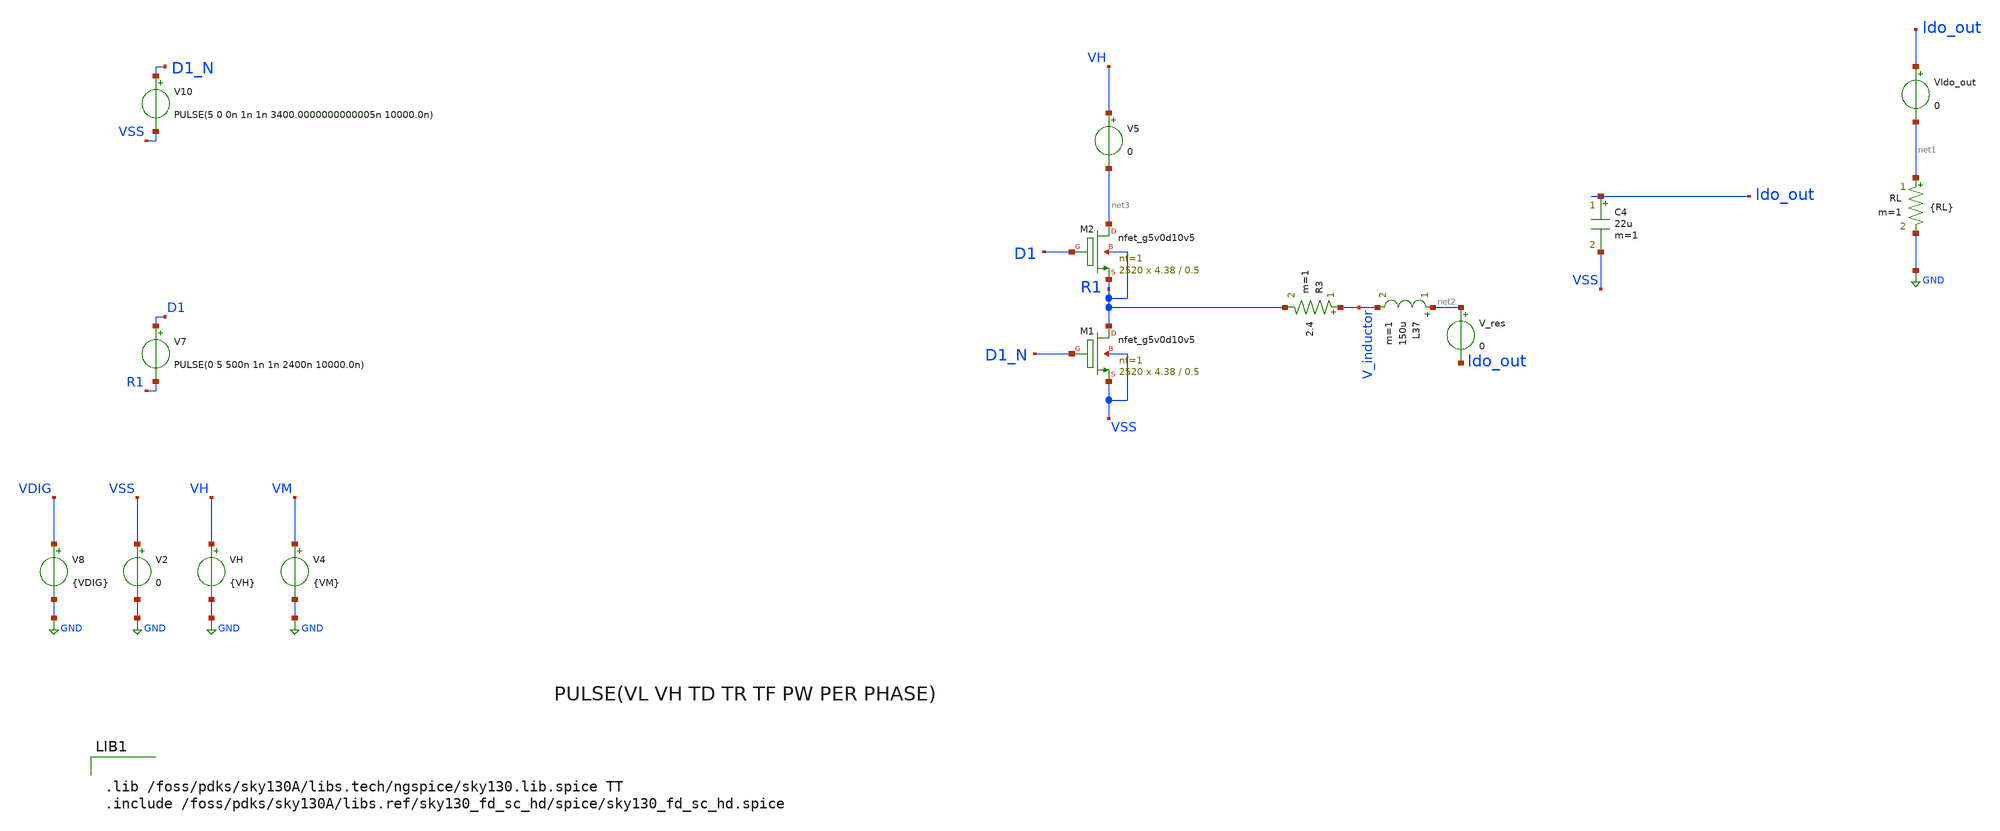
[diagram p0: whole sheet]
** sch_path: LS_boot_20230921/sch/tb_DCDC_wfilter_1core100KHznoCext_buckBOOT_eff_nols.sch
**.subckt tb_DCDC_wfilter_1core100KHznoCext_buckBOOT_eff_nols
V2 VSS GND 0
VH VH GND {VH}
V8 VDIG GND {VDIG}
V4 VM GND {VM}
C4 ldo_out VSS 22u m=1
RL net1 GND {RL} m=1
Vldo_out ldo_out net1 0
V7 D1 R1 PULSE(0 5 500n 1n 1n 2400n 10000.0n)
V10 D1_N VSS PULSE(5 0 0n 1n 1n 3400.0000000000005n 10000.0n)
L37 net2 V_inductor 150u m=1
R3 V_inductor R1 2.4 m=1
XM1 R1 D1_N VSS VSS sky130_fd_pr__nfet_g5v0d10v5 L=0.5 W=4.38 nf=1 ad='int((nf+1)/2) * W/nf * 0.29' as='int((nf+2)/2) * W/nf * 0.29'
+ pd='2*int((nf+1)/2) * (W/nf + 0.29)' ps='2*int((nf+2)/2) * (W/nf + 0.29)' nrd='0.29 / W' nrs='0.29 / W'
+ sa=0 sb=0 sd=0 mult=2520 m=2520
V5 VH net3 0
V_res net2 ldo_out 0
XM2 net3 D1 R1 R1 sky130_fd_pr__nfet_g5v0d10v5 L=0.5 W=4.38 nf=1 ad='int((nf+1)/2) * W/nf * 0.29' as='int((nf+2)/2) * W/nf * 0.29'
+ pd='2*int((nf+1)/2) * (W/nf + 0.29)' ps='2*int((nf+2)/2) * (W/nf + 0.29)' nrd='0.29 / W' nrs='0.29 / W'
+ sa=0 sb=0 sd=0 mult=2520 m=2520
**** begin user architecture code


.param VIN = 5
.param VDIG = 1.8
.param VH = 10
.param VM = 5
.param VBAT = 5
.param RL = 44
VGND VGND GND 0
VNB VNB GND 0
VPB VPB GND 1.8
VPWR VPWR GND 1.8

.option scale=1e-6
*.options itl4=25
*.options method=gear
*.option temp=80
.ic v(vout_core)=3
.ic v(V_inductor)=3
.ic v(V_res)=3
*.probe vd(MP2:G:S)
*.save all
*.save v(d1) v(d2) v(d1top_5v) v(d2_5v) v(d2bot_5v) v(d1bot_5v) v(vout) v(vout_core) v(vdd) v(vh) i(v1) i(v5) i(vmeas) v(v_cftop,v_cfbot)
.save v(D1) v(D2) v(D1_N) v(D2_N) v(VOUT_CORE) v(ldo_out) v(vh) i(v3) i(v10) i(v11) v(v_cftop,v_cfbot) v(D1,v_cftop) v(D2,vout_core) v(D2_N,v_cfbot) v(D1_Nv,VSS) v(v_out_ls1) v(v_out_ls2) v(d2_n,v_cfbot) v(D1_s) v(D2_s) v(D2_N_s) v(D1_N_s) v(V_res) i(v9) v(ldo_out)
.save v(neg) v(pos) i(vh) i(v_res) v(R1) v(Vboot) v(vfe) v(vre) v(vbat) i(vbat) v(v_inductor)
.save @m.xm4.msky130_fd_pr__nfet_g5v0d10v5[vds]
.param mc_mm_switch=0
.options savecurrents
.control
*set gmin = 1e-20
*save all
*tran 10n 3m
tran 10n 3m
*write DCDC_v1p4_5MHz_NMOS_PMOS.raw
*wrdata
*+ ~/Documents/Postdoc/chipathon2022/3LFCC_AC3E/xschem/dev_switches/DCDC_5V_FINAL/3LFCC_v1p4.txt tran.v(vout) tran.i(vmeas) tran.v(vdd) tran.i(v3) tran.v(vh) tran.i(v5)
*wrdata /foss/designs/personal/3LFCC_AC3E/xschem/hierarchy_sch/DCDC_5V_FINAL/3LFCC_v1p4.txt
*+ tran.v(vout_core) tran.i(v1)
*wrdata
*+ /foss/designs/personal/3LFCC_AC3E/xschem/testbench/TopModule/3LFCC_v1p5_topmodule_wfilter_jmtest.txt tran.v(vout_core) tran.i(v3) tran.i(v4) tran.i(v9)
*wrdata /foss/designs/personal/3LFCC_v1p5_topmodule_wfilter_onecore10MHz_3lfcc23.txt
*+ tran.v(vout_core) tran.i(v3) tran.i(v4) tran.i(v9)
wrdata /foss/designs/Open3LFCC_V2_GD12V/data/DCDCnLDO_wfilter_1core100KHznoCext_buckBOOT_eff.txt
+ tran.v(vh) tran.i(vh) tran.v(ldo_out) tran.i(vldo_out) tran.v(vbat) tran.i(vbat)




plot v(D1_N_s) v(D1_s)
plot v(D1_N)
plot v(Vboot)-v(R1)
plot i(vh)
plot i(vldo_out)
plot v(ldo_out)
plot v(vfe) v(vre)
plot i(vbat)
plot i(v_res)
plot v(V_inductor)
plot v(D1_N_s) v(D1_s) v(V_inductor) i(v_res)
plot v(R1)

plot v(D1_s) v(D1)-v(R1)
*let id20  = @m.xm20.msky130_fd_pr__nfet_g5v0d10v5[id]
*plot id20






.endc




.lib /foss/pdks/sky130A/libs.tech/ngspice/sky130.lib.spice TT
.include /foss/pdks/sky130A/libs.ref/sky130_fd_sc_hd/spice/sky130_fd_sc_hd.spice


**** end user architecture code
**.ends
.GLOBAL GND
.end
